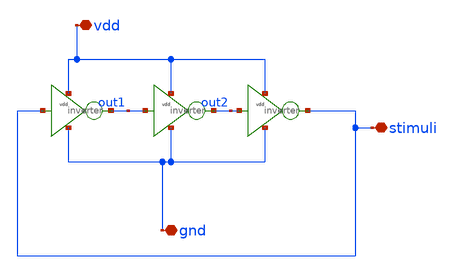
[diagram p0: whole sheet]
** sch_path: xschem/src/ring_osc/ring_osc_xschem.sch
**.subckt ring_osc_xschem vdd stimuli gnd
*.iopin vdd
*.iopin stimuli
*.iopin gnd
x1 vdd stimuli out1 gnd inverter
x2 vdd out1 out2 gnd inverter
x3 vdd out2 stimuli gnd inverter
**.ends

* expanding   symbol:  src/inverter/inverter.sym # of pins=4
** sym_path: xschem/src/inverter/inverter.sym
** sch_path: xschem/src/inverter/inverter.sch
.subckt inverter vdd A B vss
*.iopin vdd
*.iopin vss
*.ipin A
*.opin B
XM3 B A vss vss sky130_fd_pr__nfet_01v8 L=0.15 W=1 nf=1 ad='int((nf+1)/2) * W/nf * 0.29' as='int((nf+2)/2) * W/nf * 0.29'
+ pd='2*int((nf+1)/2) * (W/nf + 0.29)' ps='2*int((nf+2)/2) * (W/nf + 0.29)' nrd='0.29 / W' nrs='0.29 / W'
+ sa=0 sb=0 sd=0 mult=1 m=1
XM1 B A vdd vdd sky130_fd_pr__pfet_01v8 L=0.15 W=2 nf=1 ad='int((nf+1)/2) * W/nf * 0.29' as='int((nf+2)/2) * W/nf * 0.29'
+ pd='2*int((nf+1)/2) * (W/nf + 0.29)' ps='2*int((nf+2)/2) * (W/nf + 0.29)' nrd='0.29 / W' nrs='0.29 / W'
+ sa=0 sb=0 sd=0 mult=1 m=1
.ends

.end
